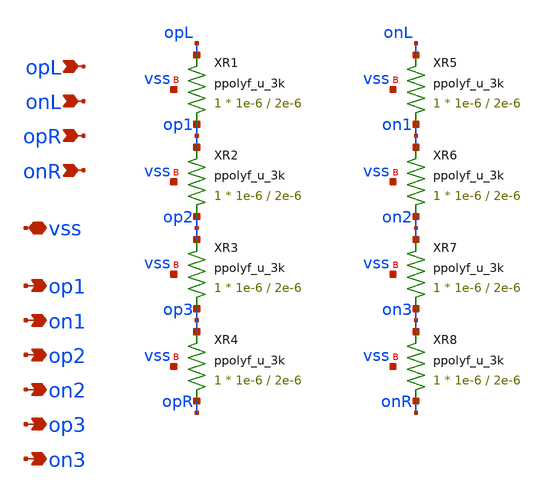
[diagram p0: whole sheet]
** sch_path: blocks/comp-array/interp4.sch
**.subckt interp4 opL onL op1 on1 opR onR op2 on2 op3 on3 vss
*.ipin opL
*.ipin onL
*.opin op1
*.opin on1
*.ipin opR
*.ipin onR
*.opin op2
*.opin on2
*.opin op3
*.opin on3
*.iopin vss
XR1 op1 opL vss ppolyf_u_3k r_width=1e-6 r_length=2e-6 m=1
XR2 op2 op1 vss ppolyf_u_3k r_width=1e-6 r_length=2e-6 m=1
XR3 op3 op2 vss ppolyf_u_3k r_width=1e-6 r_length=2e-6 m=1
XR4 opR op3 vss ppolyf_u_3k r_width=1e-6 r_length=2e-6 m=1
XR5 on1 onL vss ppolyf_u_3k r_width=1e-6 r_length=2e-6 m=1
XR6 on2 on1 vss ppolyf_u_3k r_width=1e-6 r_length=2e-6 m=1
XR7 on3 on2 vss ppolyf_u_3k r_width=1e-6 r_length=2e-6 m=1
XR8 onR on3 vss ppolyf_u_3k r_width=1e-6 r_length=2e-6 m=1
**.ends
.end
